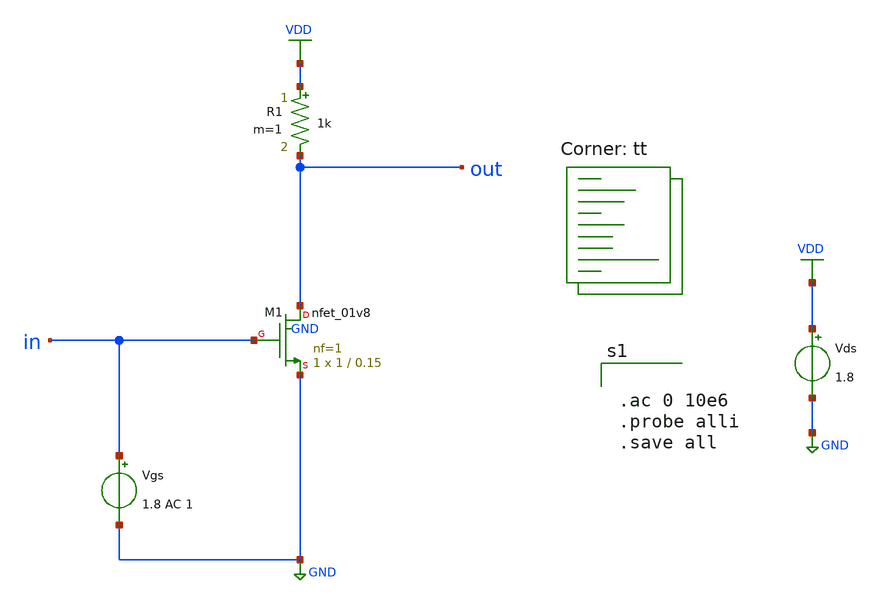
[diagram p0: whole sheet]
** sch_path: extraction.sch
**.subckt extraction
XM1 out in GND GND sky130_fd_pr__nfet_01v8 L=0.15 W=1 nf=1 ad='int((nf+1)/2) * W/nf * 0.29' as='int((nf+2)/2) * W/nf * 0.29'
+ pd='2*int((nf+1)/2) * (W/nf + 0.29)' ps='2*int((nf+2)/2) * (W/nf + 0.29)' nrd='0.29 / W' nrs='0.29 / W'
+ sa=0 sb=0 sd=0 mult=1 m=1
Vgs in GND 1.8 AC 1
Vds VDD GND 1.8
R1 VDD out 1k m=1
**** begin user architecture code


.ac 0 10e6
.probe alli
.save all

.lib $::SKYWATER_MODELS/sky130.lib.spice tt
**** end user architecture code
**.ends
.GLOBAL GND
.GLOBAL VDD
.end
